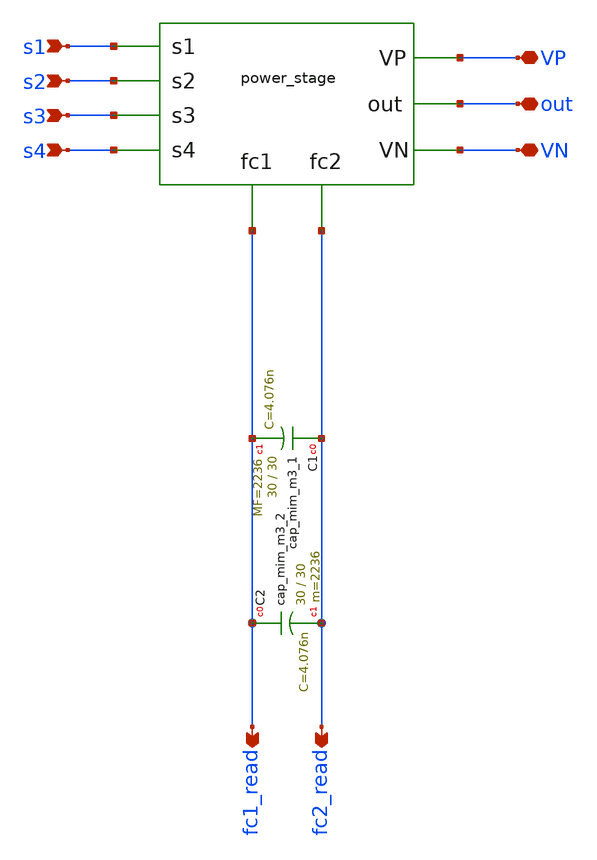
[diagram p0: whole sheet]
** sch_path: xschem/release/converter.sch
**.subckt converter s1 s2 s3 s4 VP VN fc1_read fc2_read out
*.ipin s1
*.ipin s2
*.ipin s3
*.ipin s4
*.iopin VP
*.iopin VN
*.opin fc1_read
*.opin fc2_read
*.iopin out
X1v s1 s2 s3 s4 fc1_read fc2_read out VP VN power_stage
XC1 fc2_read fc1_read sky130_fd_pr__cap_mim_m3_1 W=30 L=30 MF=2236 m=2236
XC2 fc1_read fc2_read sky130_fd_pr__cap_mim_m3_2 W=30 L=30 MF=2236 m=2236
**.ends

* expanding   symbol:  power_stage.sym # of pins=9
** sym_path: xschem/release/power_stage.sym
** sch_path: xschem/release/power_stage.sch
.subckt power_stage s1 s2 s3 s4 fc1 fc2 out VP VN
*.ipin s1
*.ipin s2
*.ipin s3
*.ipin s4
*.iopin VP
*.iopin VN
*.opin out
*.opin fc1
*.opin fc2
XM3 out s3 fc2 fc2 sky130_fd_pr__nfet_g5v0d10v5 L=0.5 W=4.38 nf=1 ad='int((nf+1)/2) * W/nf * 0.29' as='int((nf+2)/2) * W/nf * 0.29'
+ pd='2*int((nf+1)/2) * (W/nf + 0.29)' ps='2*int((nf+2)/2) * (W/nf + 0.29)' nrd='0.29 / W' nrs='0.29 / W'
+ sa=0 sb=0 sd=0 mult=2520 m=2520
XM2 out s2 fc1 fc1 sky130_fd_pr__pfet_g5v0d10v5 L=0.5 W=4.38 nf=1 ad='int((nf+1)/2) * W/nf * 0.29' as='int((nf+2)/2) * W/nf * 0.29'
+ pd='2*int((nf+1)/2) * (W/nf + 0.29)' ps='2*int((nf+2)/2) * (W/nf + 0.29)' nrd='0.29 / W' nrs='0.29 / W'
+ sa=0 sb=0 sd=0 mult=4512 m=4512
XM1 fc1 s1 VP VP sky130_fd_pr__pfet_g5v0d10v5 L=0.5 W=4.38 nf=1 ad='int((nf+1)/2) * W/nf * 0.29' as='int((nf+2)/2) * W/nf * 0.29'
+ pd='2*int((nf+1)/2) * (W/nf + 0.29)' ps='2*int((nf+2)/2) * (W/nf + 0.29)' nrd='0.29 / W' nrs='0.29 / W'
+ sa=0 sb=0 sd=0 mult=4512 m=4512
XM4 fc2 s4 VN VN sky130_fd_pr__nfet_g5v0d10v5 L=0.5 W=4.38 nf=1 ad='int((nf+1)/2) * W/nf * 0.29' as='int((nf+2)/2) * W/nf * 0.29'
+ pd='2*int((nf+1)/2) * (W/nf + 0.29)' ps='2*int((nf+2)/2) * (W/nf + 0.29)' nrd='0.29 / W' nrs='0.29 / W'
+ sa=0 sb=0 sd=0 mult=2520 m=2520
.ends

.end
